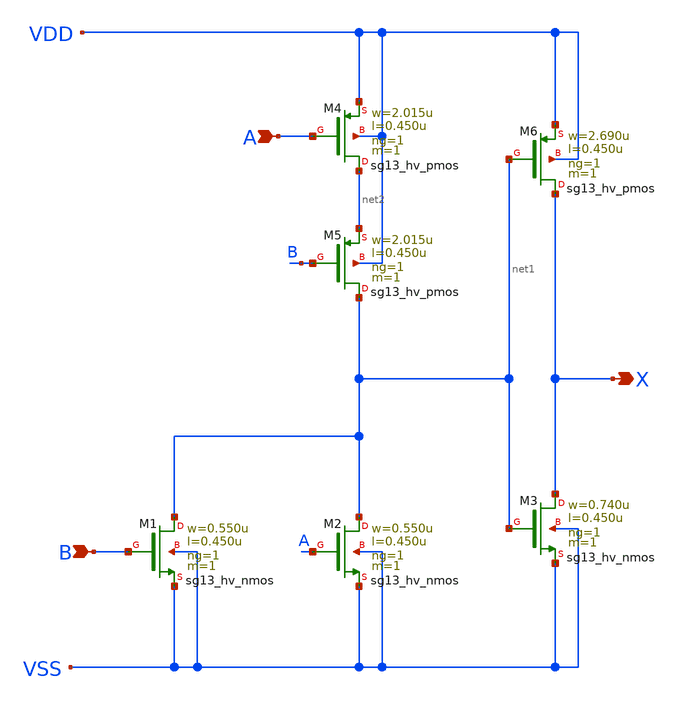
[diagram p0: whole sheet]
** sch_path: ihp-sg13g2/libs.ref/sg13g2_stdcell_hv/sch/xschem/sg13g2_hv_or2_1.sch
* Copyright 2023 IHP PDK Authors
* Licensed under the Apache License, Version 2.0 (the "License");
* you may not use this file except in compliance with the License.
* You may obtain a copy of the License at
* https://www.apache.org/licenses/LICENSE-2.0
* Unless required by applicable law or agreed to in writing, software
* distributed under the License is distributed on an "AS IS" BASIS,
* WITHOUT WARRANTIES OR CONDITIONS OF ANY KIND, either express or implied.
* See the License for the specific language governing permissions and
* limitations under the License.
**.subckt sg13g2_hv_or2_1 X B A
*.opin X
*.ipin B
*.ipin A
XM1 net1 B VSS VSS sg13_hv_nmos w=0.550u l=0.450u ng=1 m=1 mm_ok=1
XM2 net1 A VSS VSS sg13_hv_nmos w=0.550u l=0.450u ng=1 m=1 mm_ok=1
XM3 X net1 VSS VSS sg13_hv_nmos w=0.740u l=0.450u ng=1 m=1 mm_ok=1
XM4 net2 A VDD VDD sg13_hv_pmos w=2.015u l=0.450u ng=1 m=1 mm_ok=1
XM5 net1 B net2 VDD sg13_hv_pmos w=2.015u l=0.450u ng=1 m=1 mm_ok=1
XM6 X net1 VDD VDD sg13_hv_pmos w=2.690u l=0.450u ng=1 m=1 mm_ok=1
**.ends
.end
